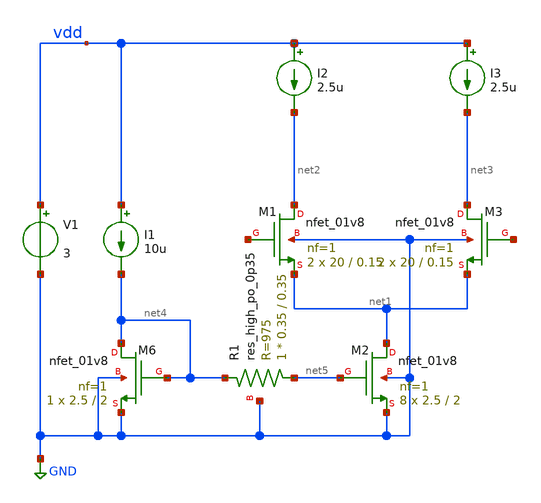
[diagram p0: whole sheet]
** sch_path: xschem/untitled.sch
**.subckt untitled
XM2 net1 net5 GND GND sky130_fd_pr__nfet_01v8 L=2 W=2.5 nf=1 ad='int((nf+1)/2) * W/nf * 0.29' as='int((nf+2)/2) * W/nf * 0.29'
+ pd='2*int((nf+1)/2) * (W/nf + 0.29)' ps='2*int((nf+2)/2) * (W/nf + 0.29)' nrd='0.29 / W' nrs='0.29 / W'
+ sa=0 sb=0 sd=0 mult=8 m=8
XM1 net2 net6 net1 GND sky130_fd_pr__nfet_01v8 L=0.15 W=20 nf=1 ad='int((nf+1)/2) * W/nf * 0.29' as='int((nf+2)/2) * W/nf * 0.29'
+ pd='2*int((nf+1)/2) * (W/nf + 0.29)' ps='2*int((nf+2)/2) * (W/nf + 0.29)' nrd='0.29 / W' nrs='0.29 / W'
+ sa=0 sb=0 sd=0 mult=2 m=2
XM3 net3 net7 net1 GND sky130_fd_pr__nfet_01v8 L=0.15 W=20 nf=1 ad='int((nf+1)/2) * W/nf * 0.29' as='int((nf+2)/2) * W/nf * 0.29'
+ pd='2*int((nf+1)/2) * (W/nf + 0.29)' ps='2*int((nf+2)/2) * (W/nf + 0.29)' nrd='0.29 / W' nrs='0.29 / W'
+ sa=0 sb=0 sd=0 mult=2 m=2
XM6 net4 net4 GND GND sky130_fd_pr__nfet_01v8 L=2 W=2.5 nf=1 ad='int((nf+1)/2) * W/nf * 0.29' as='int((nf+2)/2) * W/nf * 0.29'
+ pd='2*int((nf+1)/2) * (W/nf + 0.29)' ps='2*int((nf+2)/2) * (W/nf + 0.29)' nrd='0.29 / W' nrs='0.29 / W'
+ sa=0 sb=0 sd=0 mult=1 m=1
I1 vdd net4 10u
XR1 net5 net4 GND sky130_fd_pr__res_high_po_0p35 L=0.35 mult=1 m=1
V1 vdd GND 3
I2 vdd net2 2.5u
I3 vdd net3 2.5u
**.ends
.GLOBAL GND
.end
